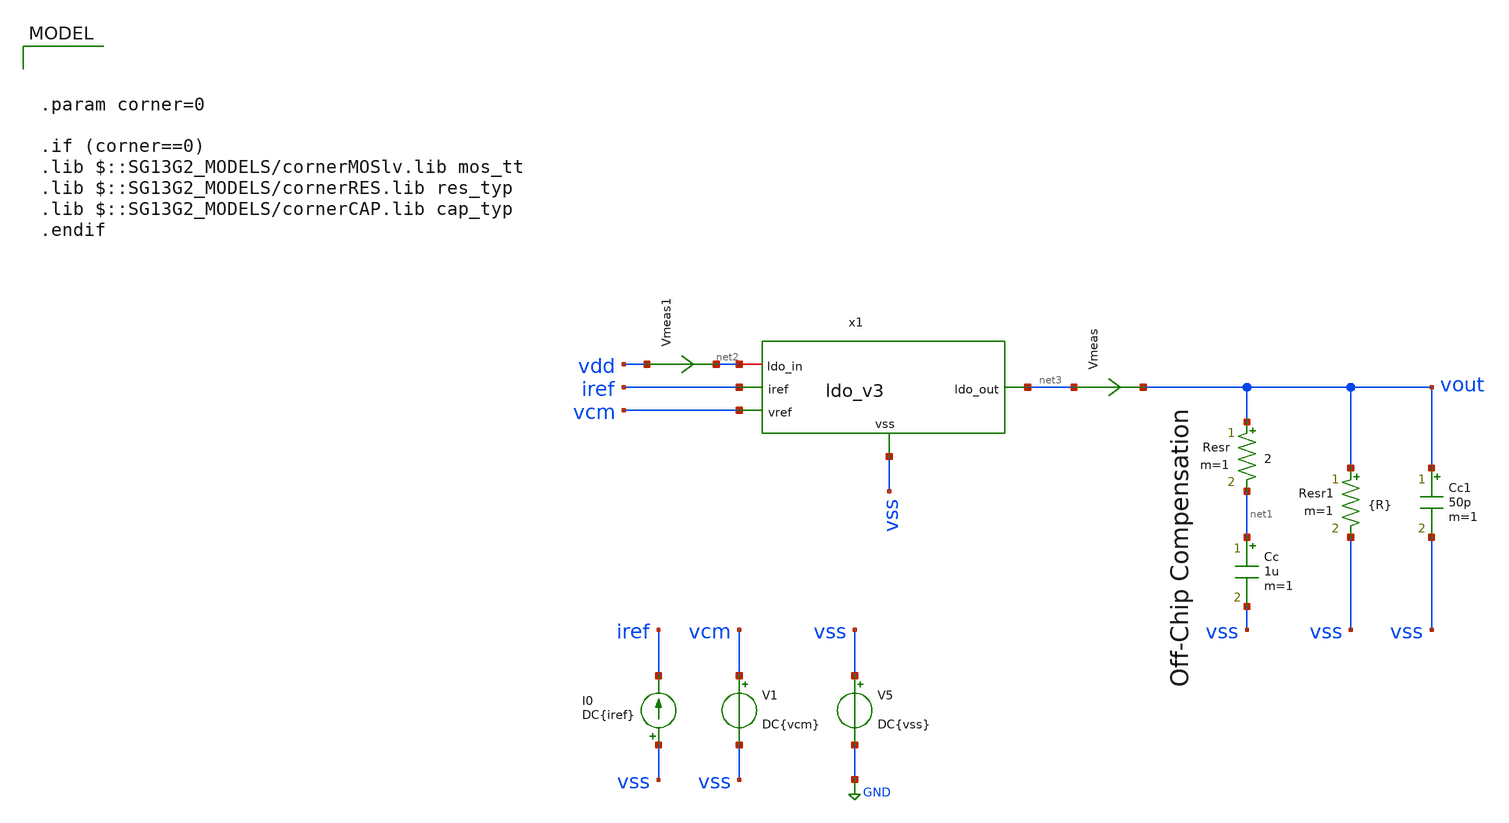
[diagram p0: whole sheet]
** sch_path: xschem/LDO/ldo_ihp_v3_tb_closeloop.sch
**.subckt ldo_ihp_v3_tb_closeloop
V1 vcm vss DC{vcm}
V5 vss GND DC{vss}
I0 vss iref DC{iref}
Vmeas net3 vout 0
.save i(vmeas)
Vmeas1 vdd net2 0
.save i(vmeas1)
Cc net1 vss 1u m=1
Resr vout net1 2 m=1
x1 net2 net3 iref vcm vss ldo_v3
Resr1 vout vss {R} m=1
Cc1 vout vss 50p m=1
**** begin user architecture code


.param corner=0

.if (corner==0)
.lib $::SG13G2_MODELS/cornerMOSlv.lib mos_tt
.lib $::SG13G2_MODELS/cornerRES.lib res_typ
.lib $::SG13G2_MODELS/cornerCAP.lib cap_typ
.endif




Vs vdd 0 1.8 AC 1
.param temp=27
.save all

.param iref = 5u
.param vdd  = 1.8
.param vss  = 0.0
.param vcm  = 0.9
.param vac  = 60m






.param R=12
*R10 vout 0 {R}
IL vout 0 PWL(0 0.1m 10u 0.1m 20u 10m 30u 10m)
*CL vout 0 50p






.control
reset
save all
set color0 = white
tran 1n 1u
plot v(vout) v(pos) v(vcm)
plot i(v.x2.vmeas1)
print @n.x2.xm1.nsg13_lv_pmos[vgs]
print @n.x2.xm1.nsg13_lv_pmos[vth]
print @n.x2.xm1.nsg13_lv_pmos[vgs]-@n.x2.xm1.nsg13_lv_pmos[vth]
print @n.x2.xm1.nsg13_lv_pmos[vds]
print @n.x2.xm1.nsg13_lv_pmos[gm]
write ldo_ihp_v3_tb_closeloop_tran.raw

.endc

.control
reset

tran 1e-6 1e-3
write test_tran.raw
noise v(vout) Vs dec 10 100 100e3
print inoise_total onoise_total
setplot noise1
plot onoise_spectrum
.endc

.end





.control
reset
save all
dc Vs 0 2.1 0.01
plot v(vout) v(vcm) v(vdd)
meas dc V_ldo_1.6 FIND v(vout) WHEN v(vdd)=1.6
meas dc V_ldo_2 FIND v(vout) WHEN v(vdd)=2
print (V_ldo_1.6-V_ldo_2)/0.4

plot deriv(vout)
let der = deriv(vout)

meas dc V_ldo_vdropout FIND v(vdd) WHEN der=0.02 CROSS=LAST
print V_ldo_vdropout-1.2

write ldo_ihp_v3_tb_closeloop_dc.raw
.endc

.end





*Simulation
.control
pre_osdi /home/ac3e/Documents/psp103_nqs.osdi
reset
  set color0 = white

  ac dec 100 1 10G
  setplot ac1
  meas ac GBW when vdb(vout)=0
  meas ac DCG find vdb(vout) at=1
  meas ac PM find vp(vout) when vdb(vout)=0
  print PM*180/PI
  meas ac GM find vdb(vout) when vp(vout)=0
  plot vdb(vout) {vp(vout)*180/PI}
  write ldo_ihp_v3_tb_closeloop_ac.raw

  reset
  op


print @n.x1.x1.xm8.nsg13_lv_nmos[vgs]-@n.x1.x1.xm8.nsg13_lv_nmos[vth]
print @n.x1.x1.xm8.nsg13_lv_nmos[vds]

print @n.x1.x1.XM7.nsg13_lv_nmos[vgs]-@n.x1.x1.XM7.nsg13_lv_nmos[vth]
print @n.x1.x1.XM7.nsg13_lv_nmos[vds]
print @n.x1.x1.XM7.nsg13_lv_nmos[ids]

print @n.x1.x1.xm6.nsg13_lv_pmos[vgs]-@n.x1.x1.xm6.nsg13_lv_pmos[vth]
print @n.x1.x1.xm6.nsg13_lv_pmos[vds]
print @n.x1.x1.xm6.nsg13_lv_pmos[gm]
print @n.x1.x1.xm6.nsg13_lv_pmos[gm]/@n.x1.x1.xm6.nsg13_lv_pmos[ids]
print @n.x1.x1.xm6.nsg13_lv_pmos[ids]

print @n.x1.x1.xm5.nsg13_lv_nmos[vgs]-@n.x1.x1.xm5.nsg13_lv_nmos[vth]
print @n.x1.x1.xm5.nsg13_lv_nmos[vds]
print @n.x1.x1.xm5.nsg13_lv_nmos[ids]

print @n.x1.x1.xm1.nsg13_lv_nmos[vgs]-@n.x1.x1.xm1.nsg13_lv_nmos[vth]
print @n.x1.x1.xm1.nsg13_lv_nmos[vds]
print @n.x1.x1.xm1.nsg13_lv_nmos[gm]

print @n.x1.x1.xm2.nsg13_lv_nmos[vgs]-@n.x1.x1.xm2.nsg13_lv_nmos[vth]
print @n.x1.x1.xm2.nsg13_lv_nmos[vds]
print @n.x1.x1.xm2.nsg13_lv_nmos[gm]

print @n.x1.x1.xm3.nsg13_lv_pmos[vgs]-@n.x1.x1.xm3.nsg13_lv_pmos[vth]
print @n.x1.x1.xm3.nsg13_lv_pmos[vds]
print @n.x1.x1.xm3.nsg13_lv_pmos[ids]

print @n.x1.x1.xm4.nsg13_lv_pmos[vgs]-@n.x1.x1.xm4.nsg13_lv_pmos[vth]
print @n.x1.x1.xm4.nsg13_lv_pmos[vds]
print @n.x1.x1.xm4.nsg13_lv_pmos[ids]

print v(vout)
print v(pos)

  setplot op1
  unset filetype
  write tb_opamp_openloop.raw

.endc

.end





.control
reset
alter IL 50u
alter R10 3600k
tran 0.1u 100u
meas TRAN V_ldo_100u FIND v(vout) AT=5u
meas TRAN V_ldo_10m FIND v(vout) AT=100u
let load_reg= V_ldo_100u-V_ldo_10m
let load_current =(-1*i(Vs)-131.8e-6)
print load_reg/9.9
plot i(Vmeas) v(vout)-1.2
write ldo_ihp_v3_tb_closeloop_load.raw
.endc

.end





.control
alter R10 36k
reset
alter @IL[pwl]=[ 0 0 10u 0 20u 0 30u 0 ]
alter @Vs[pulse]=[ 1.8 1.6 50u 1u 1u 10u 100u ]
alter IL 0
tran 0.1u 100u
plot v(vdd) v(vout)
write ldo_ihp_v3_tb_closeloop_settime.raw
.endc


.end





*Simulation
.control
dc temp -40 125 1
plot v(vout)
.endc

.end




**** end user architecture code
**.ends
.GLOBAL GND
.end
